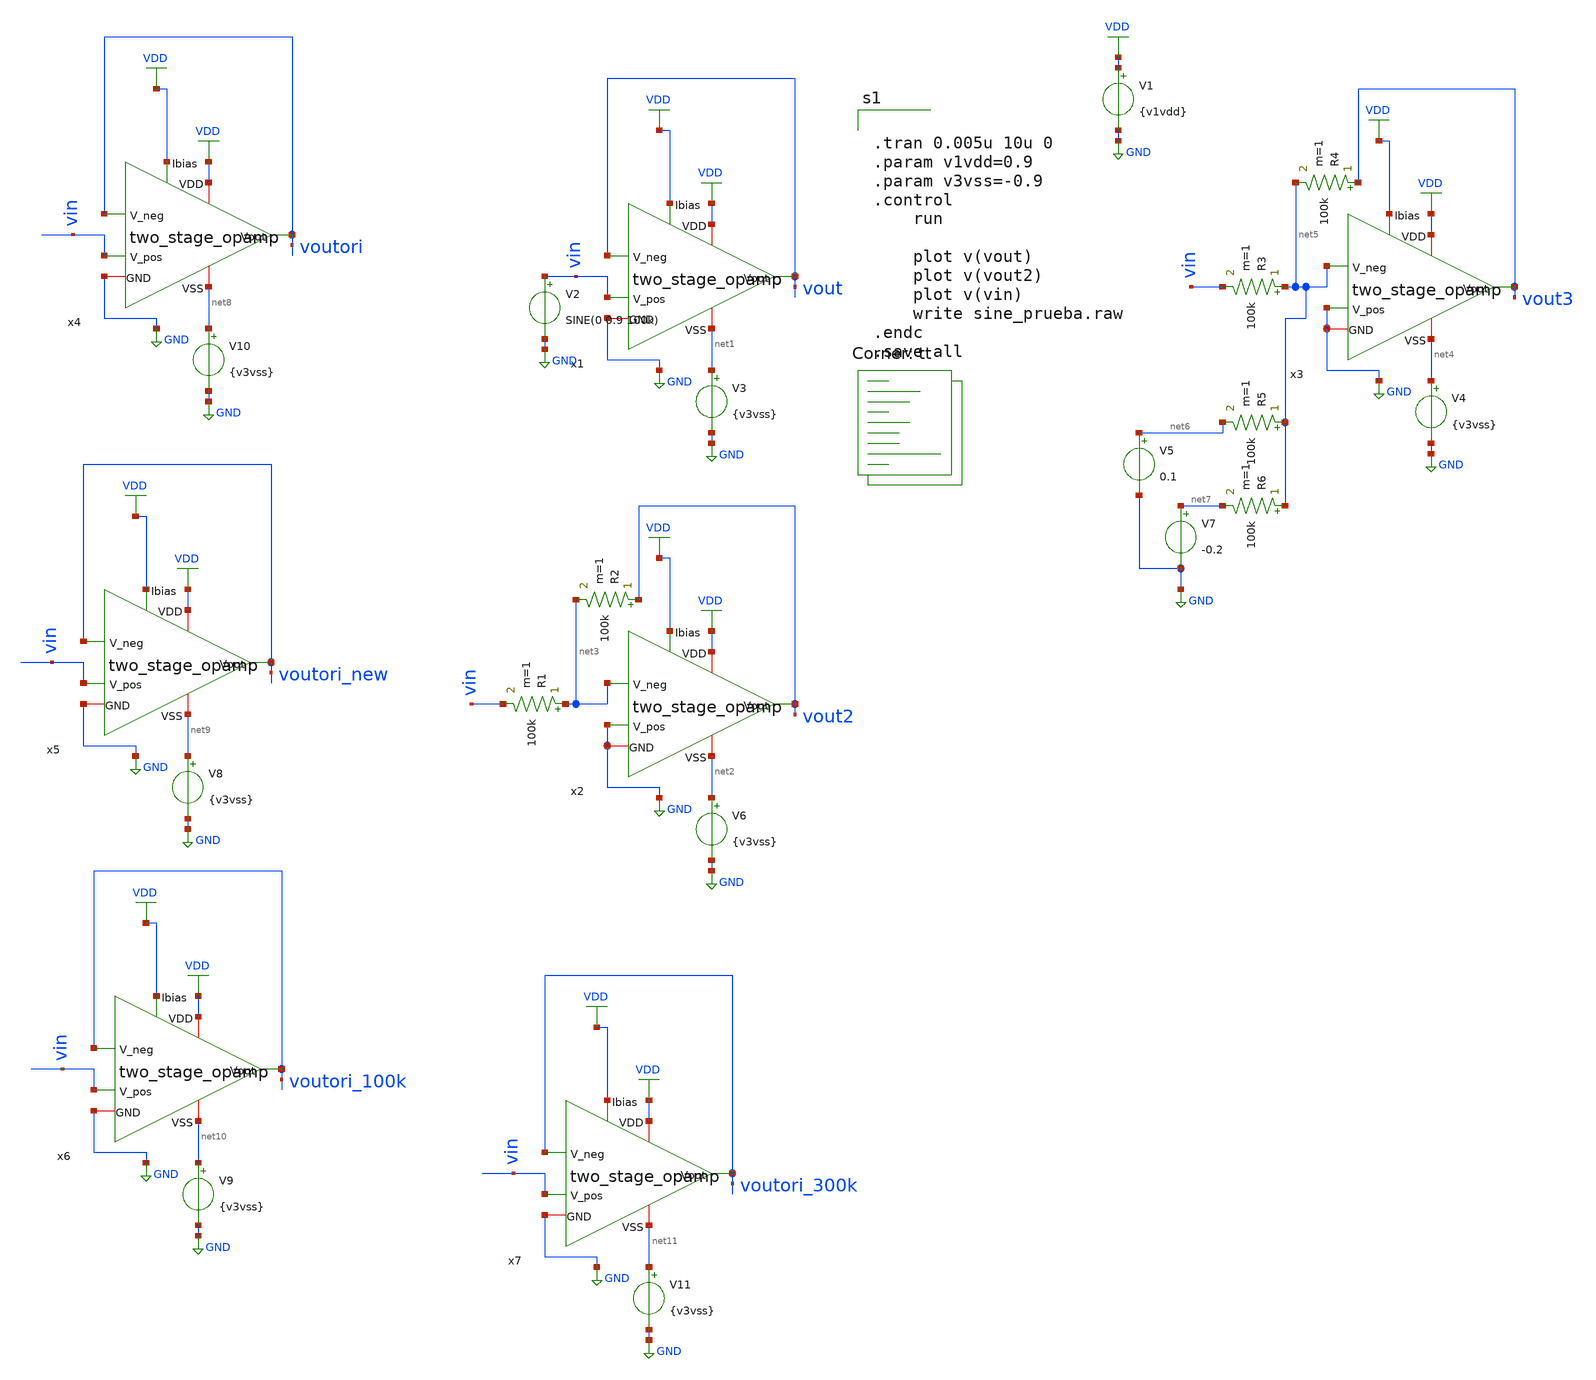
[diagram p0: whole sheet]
** sch_path: two_stage_opamp/sine_prueba.sch
**.subckt sine_prueba
x1 VDD vout VDD vout GND vin net1 two_stage_opamp W1=2.13 W2=9 W3=8.7 W4=9 W5=9.8 W6=8.7 L1=0.3965
+ L2=0.3965 L3=0.3965 L4=0.9 L5=1.2 L6=0.8
V1 VDD GND {v1vdd}
V2 vin GND SINE(0 0.9 100k)
V3 net1 GND {v3vss}
x2 VDD vout2 VDD net3 GND GND net2 two_stage_opamp W1=2.13 W2=9 W3=8.7 W4=9 W5=9.8 W6=8.7 L1=0.3965
+ L2=0.3965 L3=0.3965 L4=0.9 L5=1.2 L6=0.8
V6 net2 GND {v3vss}
R1 net3 vin 100k m=1
R2 vout2 net3 100k m=1
x3 VDD vout3 VDD net5 GND GND net4 two_stage_opamp W1=2.13 W2=9 W3=8.7 W4=9 W5=9.8 W6=8.7 L1=0.3965
+ L2=0.3965 L3=0.3965 L4=0.9 L5=1.2 L6=0.8
V4 net4 GND {v3vss}
R3 net5 vin 100k m=1
R4 vout3 net5 100k m=1
R5 net5 net6 100k m=1
R6 net5 net7 100k m=1
V5 net6 GND 0.1
V7 net7 GND -0.2
x4 VDD voutori VDD voutori GND vin net8 two_stage_opamp W1=5 W2=5 W3=3 W4=4.5 W5=4 W6=5 L1=0.15
+ L2=0.15 L3=0.15 L4=0.15 L5=3 L6=0.15
V10 net8 GND {v3vss}
x5 VDD voutori_new VDD voutori_new GND vin net9 two_stage_opamp W1=2.129 W2=9.0 W3=8.7 W4=9.0 W5=9.8
+ W6=8.7 L1=0.397 L2=0.397 L3=0.397 L4=0.9 L5=1.2 L6=0.8
V8 net9 GND {v3vss}
x6 VDD voutori_100k VDD voutori_100k GND vin net10 two_stage_opamp W1=1.875 W2=2.02 W3=2.265 W4=2.02
+ W5=2.265 W6=9.3 L1=1.623 L2=1.382 L3=0.834 L4=1.382 L5=3.8 L6=1.623
V9 net10 GND {v3vss}
x7 VDD voutori_300k VDD voutori_300k GND vin net11 two_stage_opamp W1=2.976 W2=2.402 W3=0.838
+ W4=2.976 W5=2.402 W6=0.838 L1=1.408 L2=0.754 L3=0.978 L4=1.408 L5=0.754 L6=0.978
V11 net11 GND {v3vss}
**** begin user architecture code


.tran 0.005u 10u 0
.param v1vdd=0.9
.param v3vss=-0.9
.control
	run

	plot v(vout)
	plot v(vout2)
	plot v(vin)
	write sine_prueba.raw
.endc
.save all


.lib $::SKYWATER_MODELS/sky130.lib.spice tt
**** end user architecture code
**.ends

* expanding   symbol:
*+  /home/ricardoatt/RATT_repos/Proyectos_xschem/two_stage_opamp/two_stage_opamp.sym # of pins=7
** sym_path: two_stage_opamp/two_stage_opamp.sym
** sch_path: two_stage_opamp/two_stage_opamp.sch
.subckt two_stage_opamp VDD Vout Ibias V_neg GND V_pos VSS  W1=15 W2=94 W3=3 W4=4.5 W5=14 W6=10
+ L1=0.15 L2=0.15 L3=0.15 L4=0.15 L5=0.15 L6=0.15
*.ipin Ibias
*.ipin V_neg
*.ipin V_pos
*.iopin VDD
*.iopin VSS
*.opin Vout
*.iopin GND
XM1 net2 V_neg net4 VSS sky130_fd_pr__nfet_01v8 L=L3 W=W3 nf=1 ad='int((nf+1)/2) * W/nf * 0.29' as='int((nf+2)/2) * W/nf * 0.29'
+ pd='2*int((nf+1)/2) * (W/nf + 0.29)' ps='2*int((nf+2)/2) * (W/nf + 0.29)' nrd='0.29 / W' nrs='0.29 / W'
+ sa=0 sb=0 sd=0 mult=1 m=1
XM3 net2 net2 VDD VDD sky130_fd_pr__pfet_01v8 L=L1 W=W1 nf=1 ad='int((nf+1)/2) * W/nf * 0.29' as='int((nf+2)/2) * W/nf * 0.29'
+ pd='2*int((nf+1)/2) * (W/nf + 0.29)' ps='2*int((nf+2)/2) * (W/nf + 0.29)' nrd='0.29 / W' nrs='0.29 / W'
+ sa=0 sb=0 sd=0 mult=1 m=1
XM2 net3 V_pos net4 VSS sky130_fd_pr__nfet_01v8 L=L3 W=W3 nf=1 ad='int((nf+1)/2) * W/nf * 0.29' as='int((nf+2)/2) * W/nf * 0.29'
+ pd='2*int((nf+1)/2) * (W/nf + 0.29)' ps='2*int((nf+2)/2) * (W/nf + 0.29)' nrd='0.29 / W' nrs='0.29 / W'
+ sa=0 sb=0 sd=0 mult=1 m=1
XM4 net3 net2 VDD VDD sky130_fd_pr__pfet_01v8 L=L1 W=W1 nf=1 ad='int((nf+1)/2) * W/nf * 0.29' as='int((nf+2)/2) * W/nf * 0.29'
+ pd='2*int((nf+1)/2) * (W/nf + 0.29)' ps='2*int((nf+2)/2) * (W/nf + 0.29)' nrd='0.29 / W' nrs='0.29 / W'
+ sa=0 sb=0 sd=0 mult=1 m=1
XM5 net4 net1 VSS VSS sky130_fd_pr__nfet_01v8 L=L4 W=W4 nf=1 ad='int((nf+1)/2) * W/nf * 0.29' as='int((nf+2)/2) * W/nf * 0.29'
+ pd='2*int((nf+1)/2) * (W/nf + 0.29)' ps='2*int((nf+2)/2) * (W/nf + 0.29)' nrd='0.29 / W' nrs='0.29 / W'
+ sa=0 sb=0 sd=0 mult=1 m=1
XM6 Vout net3 VDD VDD sky130_fd_pr__pfet_01v8 L=L2 W=W2 nf=1 ad='int((nf+1)/2) * W/nf * 0.29' as='int((nf+2)/2) * W/nf * 0.29'
+ pd='2*int((nf+1)/2) * (W/nf + 0.29)' ps='2*int((nf+2)/2) * (W/nf + 0.29)' nrd='0.29 / W' nrs='0.29 / W'
+ sa=0 sb=0 sd=0 mult=1 m=1
XM7 Vout net1 VSS VSS sky130_fd_pr__nfet_01v8 L=L5 W=W5 nf=1 ad='int((nf+1)/2) * W/nf * 0.29' as='int((nf+2)/2) * W/nf * 0.29'
+ pd='2*int((nf+1)/2) * (W/nf + 0.29)' ps='2*int((nf+2)/2) * (W/nf + 0.29)' nrd='0.29 / W' nrs='0.29 / W'
+ sa=0 sb=0 sd=0 mult=1 m=1
XM8 net1 net1 VSS VSS sky130_fd_pr__nfet_01v8 L=L4 W=W4 nf=1 ad='int((nf+1)/2) * W/nf * 0.29' as='int((nf+2)/2) * W/nf * 0.29'
+ pd='2*int((nf+1)/2) * (W/nf + 0.29)' ps='2*int((nf+2)/2) * (W/nf + 0.29)' nrd='0.29 / W' nrs='0.29 / W'
+ sa=0 sb=0 sd=0 mult=1 m=1
XM9 net1 net1 Ibias Ibias sky130_fd_pr__pfet_01v8 L=L6 W=W6 nf=1 ad='int((nf+1)/2) * W/nf * 0.29' as='int((nf+2)/2) * W/nf * 0.29'
+ pd='2*int((nf+1)/2) * (W/nf + 0.29)' ps='2*int((nf+2)/2) * (W/nf + 0.29)' nrd='0.29 / W' nrs='0.29 / W'
+ sa=0 sb=0 sd=0 mult=1 m=1
XC1 net3 Vout sky130_fd_pr__cap_mim_m3_1 W=10 L=1 MF=1 m=1
.ends

.GLOBAL VDD
.GLOBAL GND
.end
